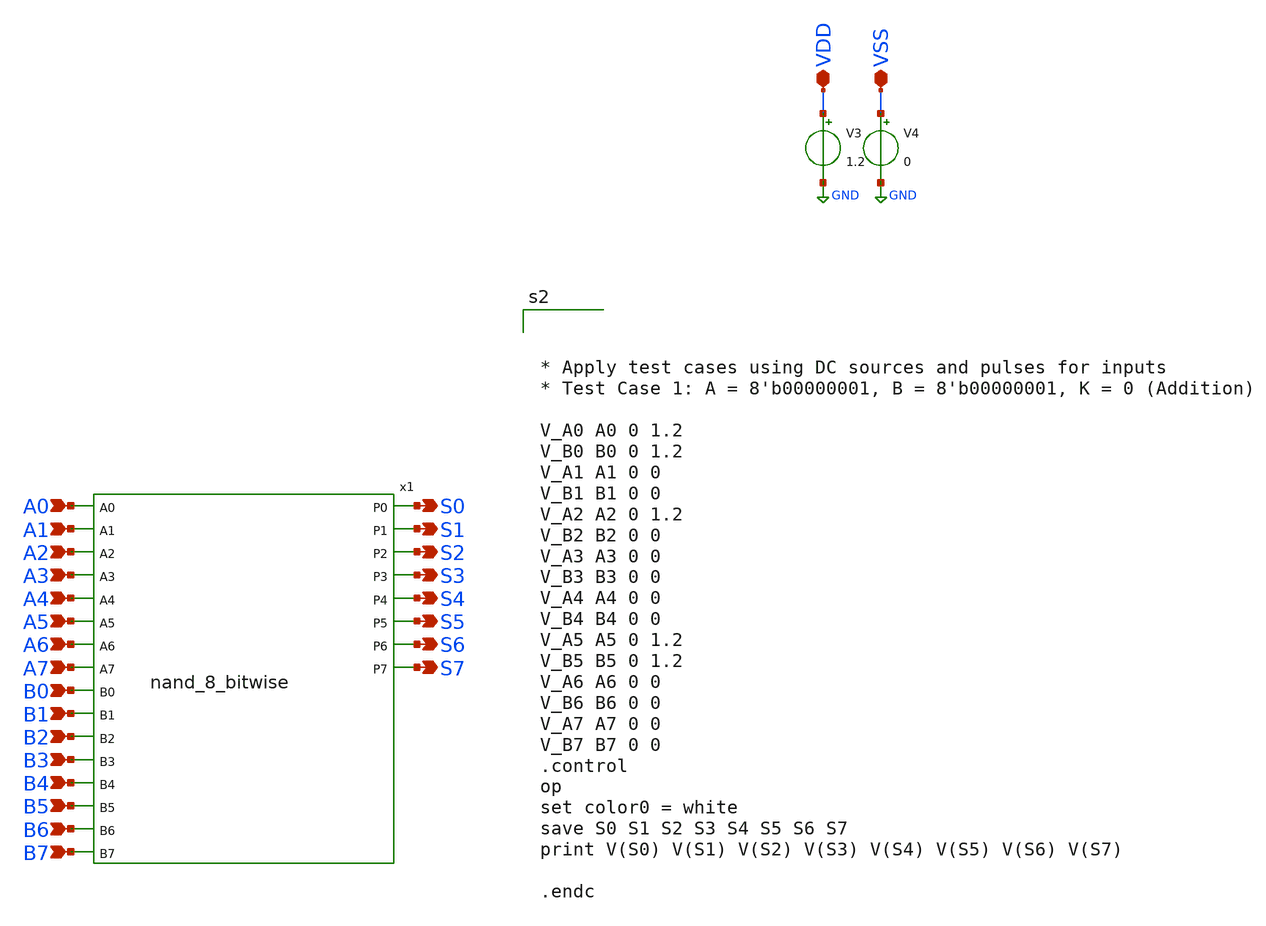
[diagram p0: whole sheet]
** sch_path: design/xschem/TEST_BENCHES/NAND8_TB.sch
**.subckt NAND8_TB A0 A1 B1 A2 B2 A3 B3 A4 B4 A5 B5 A6 B6 A7 B7 B0 VDD VSS S6 S7 S3 S4 S5 S0 S1 S2
*.ipin A0
*.ipin A1
*.ipin B1
*.ipin A2
*.ipin B2
*.ipin A3
*.ipin B3
*.ipin A4
*.ipin B4
*.ipin A5
*.ipin B5
*.ipin A6
*.ipin B6
*.ipin A7
*.ipin B7
*.ipin B0
*.iopin VDD
*.iopin VSS
*.opin S6
*.opin S7
*.opin S3
*.opin S4
*.opin S5
*.opin S0
*.opin S1
*.opin S2
x1 A0 A1 A2 A3 A4 A5 A6 A7 B0 B1 B2 B3 B4 B5 B6 B7 S0 S1 S2 S3 S4 S5 S6 S7 nand_8_bitwise
V3 VDD GND 1.2
V4 VSS GND 0
**** begin user architecture code



* Apply test cases using DC sources and pulses for inputs
* Test Case 1: A = 8'b00000001, B = 8'b00000001, K = 0 (Addition)

V_A0 A0 0 1.2
V_B0 B0 0 1.2
V_A1 A1 0 0
V_B1 B1 0 0
V_A2 A2 0 1.2
V_B2 B2 0 0
V_A3 A3 0 0
V_B3 B3 0 0
V_A4 A4 0 0
V_B4 B4 0 0
V_A5 A5 0 1.2
V_B5 B5 0 1.2
V_A6 A6 0 0
V_B6 B6 0 0
V_A7 A7 0 0
V_B7 B7 0 0
.control
op
set color0 = white
save S0 S1 S2 S3 S4 S5 S6 S7
print V(S0) V(S1) V(S2) V(S3) V(S4) V(S5) V(S6) V(S7)

.endc



** opencircuitdesign pdks install
.lib $::SKYWATER_MODELS/sky130.lib.spice tt_mm


**** end user architecture code
**.ends

* expanding   symbol:  NAND/nand_8_bitwise.sym # of pins=24
** sym_path: design/xschem/NAND/nand_8_bitwise.sym
** sch_path: design/xschem/NAND/nand_8_bitwise.sch
.subckt nand_8_bitwise A0 A1 A2 A3 A4 A5 A6 A7 B0 B1 B2 B3 B4 B5 B6 B7 P0 P1 P2 P3 P4 P5 P6 P7
*.ipin B7
*.ipin B5
*.ipin B6
*.ipin B4
*.ipin B3
*.ipin B2
*.ipin B1
*.ipin B0
*.opin P7
*.opin P6
*.opin P5
*.opin P4
*.opin P3
*.opin P2
*.opin P1
*.opin P0
*.ipin A7
*.ipin A5
*.ipin A6
*.ipin A4
*.ipin A3
*.ipin A2
*.ipin A1
*.ipin A0
x1 B7 A7 VSS VDD P7 nand2
x2 B6 A6 VSS VDD P6 nand2
x3 B5 A5 VSS VDD P5 nand2
x4 B4 A4 VSS VDD P4 nand2
x5 B3 A3 VSS VDD P3 nand2
x6 B2 A2 VSS VDD P2 nand2
x7 B1 A1 VSS VDD P1 nand2
x8 B0 A0 VSS VDD P0 nand2
.ends


* expanding   symbol:  NAND/nand2.sym # of pins=3
** sym_path: design/xschem/NAND/nand2.sym
** sch_path: design/xschem/NAND/nand2.sch
.subckt nand2 A B VSS VDD Y
*.ipin A
*.opin Y
*.ipin B
XM1 Y A VDD VDD sky130_fd_pr__pfet_01v8 L=0.15 W=3.2 nf=1 ad='int((nf+1)/2) * W/nf * 0.29' as='int((nf+2)/2) * W/nf * 0.29'
+ pd='2*int((nf+1)/2) * (W/nf + 0.29)' ps='2*int((nf+2)/2) * (W/nf + 0.29)' nrd='0.29 / W' nrs='0.29 / W'
+ sa=0 sb=0 sd=0 mult=1 m=1
XM2 Y A net1 net1 sky130_fd_pr__nfet_01v8 L=0.15 W=2 nf=1 ad='int((nf+1)/2) * W/nf * 0.29' as='int((nf+2)/2) * W/nf * 0.29'
+ pd='2*int((nf+1)/2) * (W/nf + 0.29)' ps='2*int((nf+2)/2) * (W/nf + 0.29)' nrd='0.29 / W' nrs='0.29 / W'
+ sa=0 sb=0 sd=0 mult=1 m=1
XM3 net1 B VSS VSS sky130_fd_pr__nfet_01v8 L=0.15 W=2 nf=1 ad='int((nf+1)/2) * W/nf * 0.29' as='int((nf+2)/2) * W/nf * 0.29'
+ pd='2*int((nf+1)/2) * (W/nf + 0.29)' ps='2*int((nf+2)/2) * (W/nf + 0.29)' nrd='0.29 / W' nrs='0.29 / W'
+ sa=0 sb=0 sd=0 mult=1 m=1
XM4 Y B VDD VDD sky130_fd_pr__pfet_01v8 L=0.15 W=3.2 nf=1 ad='int((nf+1)/2) * W/nf * 0.29' as='int((nf+2)/2) * W/nf * 0.29'
+ pd='2*int((nf+1)/2) * (W/nf + 0.29)' ps='2*int((nf+2)/2) * (W/nf + 0.29)' nrd='0.29 / W' nrs='0.29 / W'
+ sa=0 sb=0 sd=0 mult=1 m=1
.ends

.GLOBAL GND
.end
